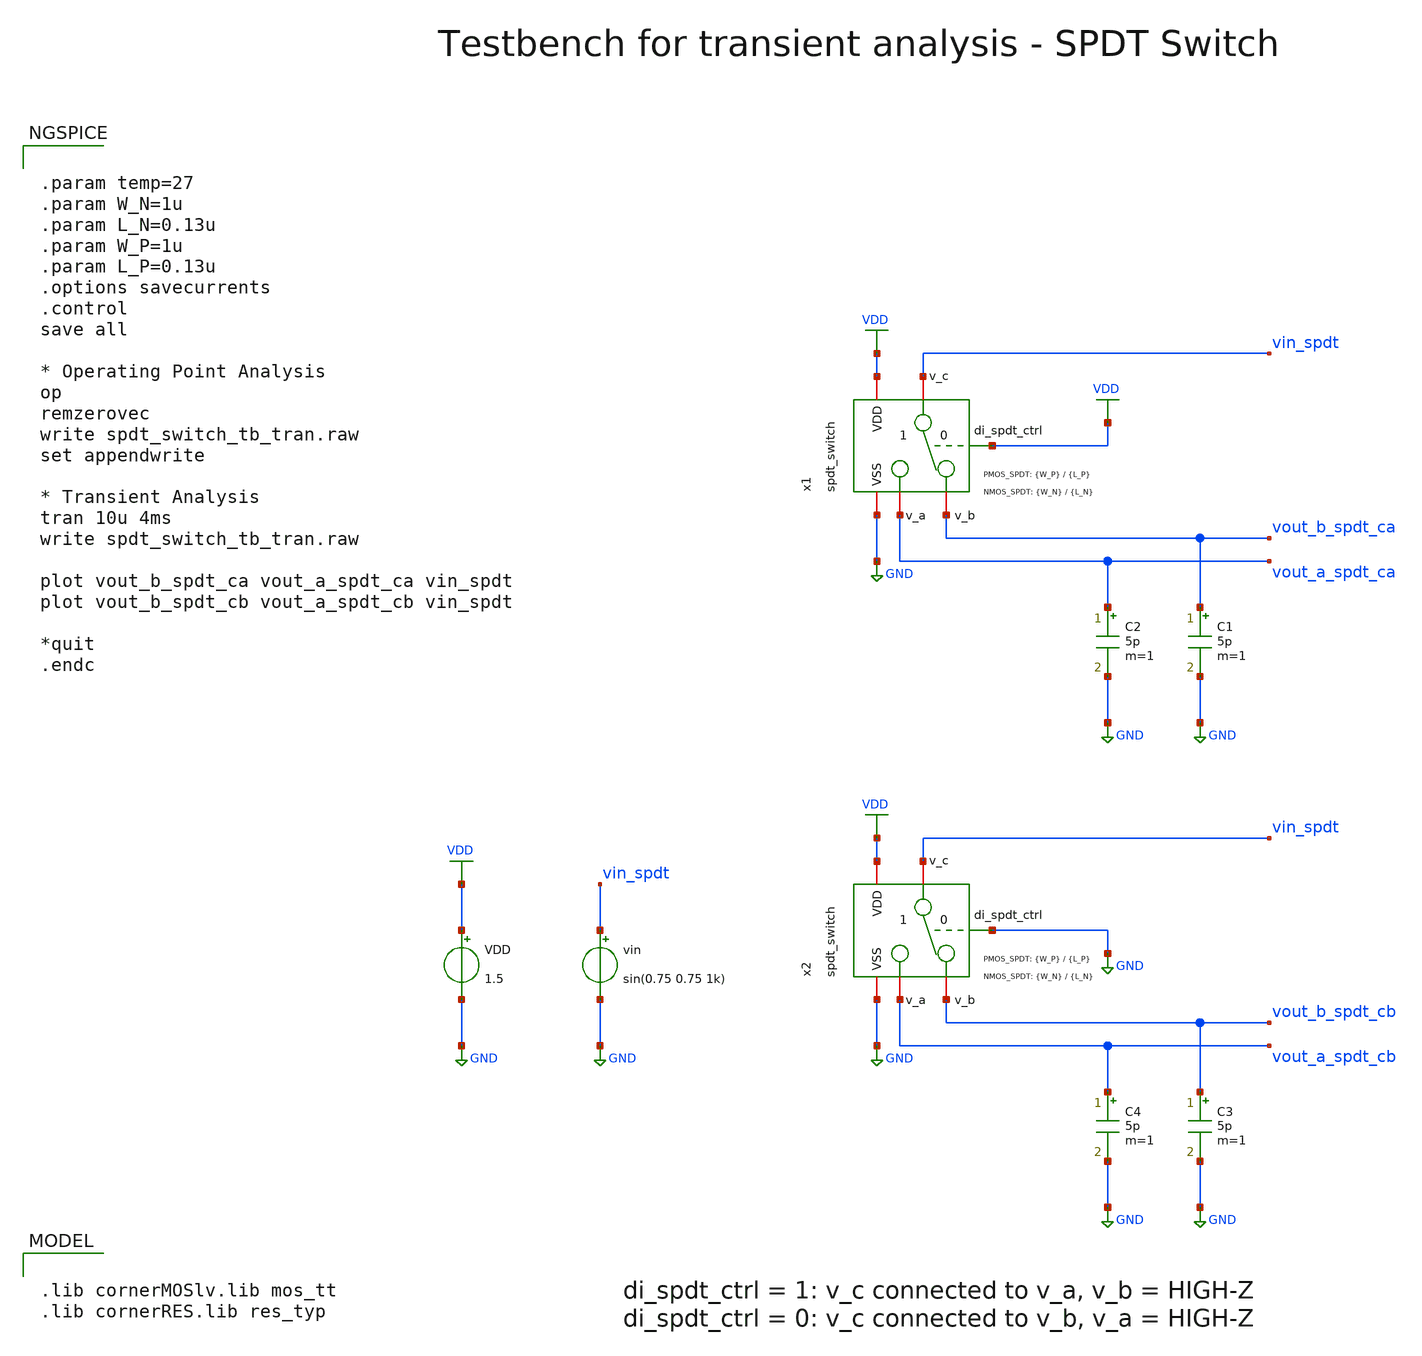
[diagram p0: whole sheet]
** sch_path: SG13G2_ATBS-ADC-main/xschem/spdt_switch/testbenches/spdt_switch_tb_tran.sch
**.subckt spdt_switch_tb_tran
C1 vout_b_spdt_ca GND 5p m=1
VDD VDD GND 1.5
vin vin_spdt GND sin(0.75 0.75 1k)
C2 vout_a_spdt_ca GND 5p m=1
C3 vout_b_spdt_cb GND 5p m=1
C4 vout_a_spdt_cb GND 5p m=1
x1 VDD VDD GND vin_spdt vout_b_spdt_ca vout_a_spdt_ca spdt_switch W_P_TG={W_P} L_P_TG={L_P} W_N_TG={W_N}
+ L_N_TG={L_N}
x2 VDD GND GND vin_spdt vout_b_spdt_cb vout_a_spdt_cb spdt_switch W_P_TG={W_P} L_P_TG={L_P} W_N_TG={W_N}
+ L_N_TG={L_N}
**** begin user architecture code

.lib cornerMOSlv.lib mos_tt
.lib cornerRES.lib res_typ



.param temp=27
.param W_N=1u
.param L_N=0.13u
.param W_P=1u
.param L_P=0.13u
.options savecurrents
.control
save all

* Operating Point Analysis
op
remzerovec
write spdt_switch_tb_tran.raw
set appendwrite

* Transient Analysis
tran 10u 4ms
write spdt_switch_tb_tran.raw

plot vout_b_spdt_ca vout_a_spdt_ca vin_spdt
plot vout_b_spdt_cb vout_a_spdt_cb vin_spdt

*quit
.endc

**** end user architecture code
**.ends

* expanding   symbol:  spdt_switch/spdt_switch.sym # of pins=6
** sym_path: SG13G2_ATBS-ADC-main/xschem/spdt_switch/spdt_switch.sym
** sch_path: SG13G2_ATBS-ADC-main/xschem/spdt_switch/spdt_switch.sch
.subckt spdt_switch VDD di_spdt_ctrl VSS v_c v_b v_a  W_P_TG=3.0u L_P_TG=0.13u W_N_TG=1.0u
+ L_N_TG=0.13u
*.iopin v_a
*.iopin v_b
*.iopin v_c
*.iopin VDD
*.iopin VSS
*.ipin di_spdt_ctrl
x1 VDD di_spdt_ctrl VSS v_c v_a di_spdt_ctrl_n transmission_gate_lv_wo_dummy W_P=W_P_TG L_P=L_P_TG
+ W_N=W_N_TG L_N=L_N_TG
x2 VDD di_spdt_ctrl_n VSS v_b v_c di_spdt_ctrl transmission_gate_lv_wo_dummy W_P=W_P_TG L_P=L_P_TG
+ W_N=W_N_TG L_N=L_N_TG
x8 VDD di_spdt_ctrl di_spdt_ctrl_n VSS inverter_lv W_P=W_P_TG L_P=L_P_TG W_N=W_N_TG L_N=L_N_TG
.ends


* expanding   symbol:  transmission_gate/transmission_gate_lv_wo_dummy.sym # of pins=6
** sym_path: SG13G2_ATBS-ADC-main/xschem/transmission_gate/transmission_gate_lv_wo_dummy.sym
** sch_path: SG13G2_ATBS-ADC-main/xschem/transmission_gate/transmission_gate_lv_wo_dummy.sch
.subckt transmission_gate_lv_wo_dummy VDD di_tg_ctrl VSS v_b v_a di_tg_ctrl_n  W_P=1.0u L_P=0.13u
+ W_N=1.0u L_N=0.13u
*.iopin v_a
*.iopin v_b
*.iopin VDD
*.iopin VSS
*.ipin di_tg_ctrl
*.ipin di_tg_ctrl_n
XM1 v_a di_tg_ctrl v_b VSS sg13_lv_nmos w=W_N l=L_N ng=1 m=1 mm_ok=1
XM2 v_a di_tg_ctrl_n v_b VDD sg13_lv_pmos w=W_P l=L_P ng=1 m=1 mm_ok=1
.ends


* expanding   symbol:  inverter/inverter_lv.sym # of pins=4
** sym_path: SG13G2_ATBS-ADC-main/xschem/inverter/inverter_lv.sym
** sch_path: SG13G2_ATBS-ADC-main/xschem/inverter/inverter_lv.sch
.subckt inverter_lv VDD vin vout VSS  W_P=3.0u L_P=0.13u W_N=1.0u L_N=0.13u
*.ipin vin
*.iopin VDD
*.iopin VSS
*.opin vout
XM1 vout vin VDD VDD sg13_lv_pmos w=W_P l=L_P ng=1 m=1 mm_ok=1
XM2 vout vin VSS VSS sg13_lv_nmos w=W_N l=L_N ng=1 m=1 mm_ok=1
.ends

.GLOBAL VDD
.GLOBAL GND
.end
